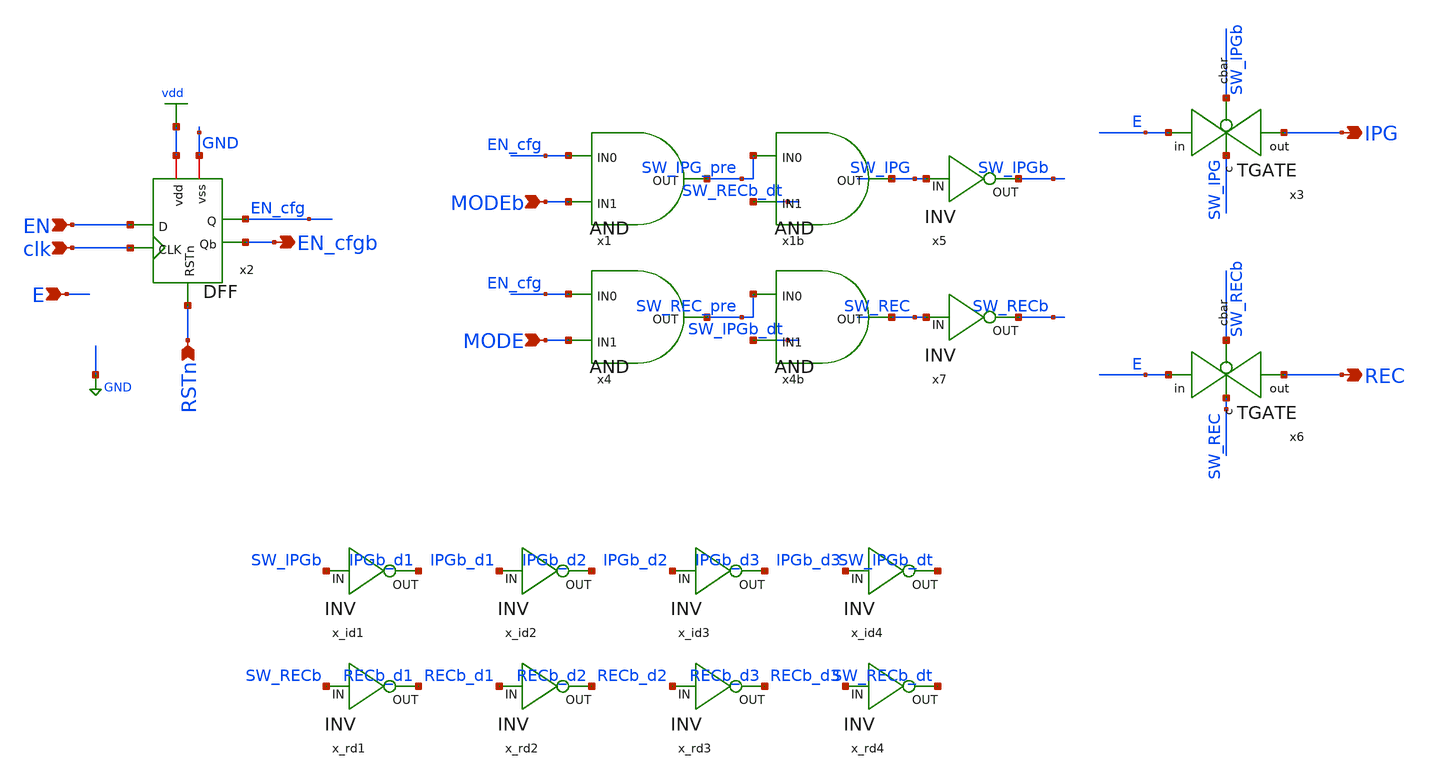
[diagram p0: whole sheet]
** sch_path: row_fixed_dt.sch
**.subckt row_fixed_dt EN clk MODEb MODE E IPG REC RSTn EN_cfgb
*.ipin EN
*.ipin clk
*.ipin MODEb
*.ipin MODE
*.ipin E
*.opin IPG
*.opin REC
*.ipin RSTn
*.opin EN_cfgb
x1 EN_cfg SW_IPG_pre MODEb AND
x2 vdd RSTn EN EN_cfg EN_cfgb clk GND DFF
x3 IPG SW_IPG SW_IPGb E TGATE
x4 EN_cfg SW_REC_pre MODE AND
x6 REC SW_REC SW_RECb E TGATE
x5 SW_IPGb SW_IPG INV
x7 SW_RECb SW_REC INV
x1b SW_IPG_pre SW_IPG SW_RECb_dt AND
x4b SW_REC_pre SW_REC SW_IPGb_dt AND
x_id1 IPGb_d1 SW_IPGb INV
x_id2 IPGb_d2 IPGb_d1 INV
x_id3 IPGb_d3 IPGb_d2 INV
x_id4 SW_IPGb_dt IPGb_d3 INV
x_rd1 RECb_d1 SW_RECb INV
x_rd2 RECb_d2 RECb_d1 INV
x_rd3 RECb_d3 RECb_d2 INV
x_rd4 SW_RECb_dt RECb_d3 INV
**.ends

* expanding   symbol:  AND/AND.sym # of pins=3
** sym_path: AND/AND.sym
** sch_path: AND/AND.sch
.subckt AND IN0 OUT IN1
*.opin OUT
*.ipin IN0
*.ipin IN1
XM1 net1 IN0 net2 GND nfet_03v3 L=0.28u W=1u nf=1 ad='int((nf+1)/2) * W/nf * 0.18u' as='int((nf+2)/2) * W/nf * 0.18u'
+ pd='2*int((nf+1)/2) * (W/nf + 0.18u)' ps='2*int((nf+2)/2) * (W/nf + 0.18u)' nrd='0.18u / W' nrs='0.18u / W'
+ sa=0 sb=0 sd=0 m=1
XM2 net2 IN1 GND GND nfet_03v3 L=0.28u W=1u nf=1 ad='int((nf+1)/2) * W/nf * 0.18u' as='int((nf+2)/2) * W/nf * 0.18u'
+ pd='2*int((nf+1)/2) * (W/nf + 0.18u)' ps='2*int((nf+2)/2) * (W/nf + 0.18u)' nrd='0.18u / W' nrs='0.18u / W'
+ sa=0 sb=0 sd=0 m=1
XM3 net1 IN0 vdd vdd pfet_03v3 L=0.28u W=1u nf=1 ad='int((nf+1)/2) * W/nf * 0.18u' as='int((nf+2)/2) * W/nf * 0.18u'
+ pd='2*int((nf+1)/2) * (W/nf + 0.18u)' ps='2*int((nf+2)/2) * (W/nf + 0.18u)' nrd='0.18u / W' nrs='0.18u / W'
+ sa=0 sb=0 sd=0 m=1
XM4 net1 IN1 vdd vdd pfet_03v3 L=0.28u W=1u nf=1 ad='int((nf+1)/2) * W/nf * 0.18u' as='int((nf+2)/2) * W/nf * 0.18u'
+ pd='2*int((nf+1)/2) * (W/nf + 0.18u)' ps='2*int((nf+2)/2) * (W/nf + 0.18u)' nrd='0.18u / W' nrs='0.18u / W'
+ sa=0 sb=0 sd=0 m=1
x1 OUT net1 INV
.ends


* expanding   symbol:  DFF/DFF.sym # of pins=7
** sym_path: DFF/DFF.sym
** sch_path: DFF/DFF.sch
.subckt DFF vdd RSTn D Q Qb CLK vss
*.ipin D
*.ipin CLK
*.ipin RSTn
*.opin Q
*.iopin vdd
*.iopin vss
*.opin Qb
XM1 net1 D net3 vss nfet_03v3 L=0.28u W=1u nf=1 ad='int((nf+1)/2) * W/nf * 0.18u' as='int((nf+2)/2) * W/nf * 0.18u'
+ pd='2*int((nf+1)/2) * (W/nf + 0.18u)' ps='2*int((nf+2)/2) * (W/nf + 0.18u)' nrd='0.18u / W' nrs='0.18u / W'
+ sa=0 sb=0 sd=0 m=1
XM2 net1 D net2 vdd pfet_03v3 L=0.28u W=1u nf=1 ad='int((nf+1)/2) * W/nf * 0.18u' as='int((nf+2)/2) * W/nf * 0.18u'
+ pd='2*int((nf+1)/2) * (W/nf + 0.18u)' ps='2*int((nf+2)/2) * (W/nf + 0.18u)' nrd='0.18u / W' nrs='0.18u / W'
+ sa=0 sb=0 sd=0 m=1
XM3 net2 c vdd vdd pfet_03v3 L=0.28u W=1u nf=1 ad='int((nf+1)/2) * W/nf * 0.18u' as='int((nf+2)/2) * W/nf * 0.18u'
+ pd='2*int((nf+1)/2) * (W/nf + 0.18u)' ps='2*int((nf+2)/2) * (W/nf + 0.18u)' nrd='0.18u / W' nrs='0.18u / W'
+ sa=0 sb=0 sd=0 m=1
XM4 net3 cbar vss vss nfet_03v3 L=0.28u W=1u nf=1 ad='int((nf+1)/2) * W/nf * 0.18u' as='int((nf+2)/2) * W/nf * 0.18u'
+ pd='2*int((nf+1)/2) * (W/nf + 0.18u)' ps='2*int((nf+2)/2) * (W/nf + 0.18u)' nrd='0.18u / W' nrs='0.18u / W'
+ sa=0 sb=0 sd=0 m=1
XM5 cbar CLK vss vss nfet_03v3 L=0.28u W=1u nf=1 ad='int((nf+1)/2) * W/nf * 0.18u' as='int((nf+2)/2) * W/nf * 0.18u'
+ pd='2*int((nf+1)/2) * (W/nf + 0.18u)' ps='2*int((nf+2)/2) * (W/nf + 0.18u)' nrd='0.18u / W' nrs='0.18u / W'
+ sa=0 sb=0 sd=0 m=1
XM6 cbar CLK vdd vdd pfet_03v3 L=0.28u W=1u nf=1 ad='int((nf+1)/2) * W/nf * 0.18u' as='int((nf+2)/2) * W/nf * 0.18u'
+ pd='2*int((nf+1)/2) * (W/nf + 0.18u)' ps='2*int((nf+2)/2) * (W/nf + 0.18u)' nrd='0.18u / W' nrs='0.18u / W'
+ sa=0 sb=0 sd=0 m=1
XM7 c cbar vss vss nfet_03v3 L=0.28u W=1u nf=1 ad='int((nf+1)/2) * W/nf * 0.18u' as='int((nf+2)/2) * W/nf * 0.18u'
+ pd='2*int((nf+1)/2) * (W/nf + 0.18u)' ps='2*int((nf+2)/2) * (W/nf + 0.18u)' nrd='0.18u / W' nrs='0.18u / W'
+ sa=0 sb=0 sd=0 m=1
XM8 c cbar vdd vdd pfet_03v3 L=0.28u W=1u nf=1 ad='int((nf+1)/2) * W/nf * 0.18u' as='int((nf+2)/2) * W/nf * 0.18u'
+ pd='2*int((nf+1)/2) * (W/nf + 0.18u)' ps='2*int((nf+2)/2) * (W/nf + 0.18u)' nrd='0.18u / W' nrs='0.18u / W'
+ sa=0 sb=0 sd=0 m=1
XM11 net5 RSTn net4 vss nfet_03v3 L=0.28u W=1u nf=1 ad='int((nf+1)/2) * W/nf * 0.18u' as='int((nf+2)/2) * W/nf * 0.18u'
+ pd='2*int((nf+1)/2) * (W/nf + 0.18u)' ps='2*int((nf+2)/2) * (W/nf + 0.18u)' nrd='0.18u / W' nrs='0.18u / W'
+ sa=0 sb=0 sd=0 m=1
XM12 net4 net6 vss vss nfet_03v3 L=0.28u W=1u nf=1 ad='int((nf+1)/2) * W/nf * 0.18u' as='int((nf+2)/2) * W/nf * 0.18u'
+ pd='2*int((nf+1)/2) * (W/nf + 0.18u)' ps='2*int((nf+2)/2) * (W/nf + 0.18u)' nrd='0.18u / W' nrs='0.18u / W'
+ sa=0 sb=0 sd=0 m=1
XM13 net5 RSTn vdd vdd pfet_03v3 L=0.28u W=1u nf=1 ad='int((nf+1)/2) * W/nf * 0.18u' as='int((nf+2)/2) * W/nf * 0.18u'
+ pd='2*int((nf+1)/2) * (W/nf + 0.18u)' ps='2*int((nf+2)/2) * (W/nf + 0.18u)' nrd='0.18u / W' nrs='0.18u / W'
+ sa=0 sb=0 sd=0 m=1
XM14 net5 net6 vdd vdd pfet_03v3 L=0.28u W=1u nf=1 ad='int((nf+1)/2) * W/nf * 0.18u' as='int((nf+2)/2) * W/nf * 0.18u'
+ pd='2*int((nf+1)/2) * (W/nf + 0.18u)' ps='2*int((nf+2)/2) * (W/nf + 0.18u)' nrd='0.18u / W' nrs='0.18u / W'
+ sa=0 sb=0 sd=0 m=1
XM15 net6 net1 vss vss nfet_03v3 L=0.28u W=1u nf=1 ad='int((nf+1)/2) * W/nf * 0.18u' as='int((nf+2)/2) * W/nf * 0.18u'
+ pd='2*int((nf+1)/2) * (W/nf + 0.18u)' ps='2*int((nf+2)/2) * (W/nf + 0.18u)' nrd='0.18u / W' nrs='0.18u / W'
+ sa=0 sb=0 sd=0 m=1
XM16 net6 net1 vdd vdd pfet_03v3 L=0.28u W=1u nf=1 ad='int((nf+1)/2) * W/nf * 0.18u' as='int((nf+2)/2) * W/nf * 0.18u'
+ pd='2*int((nf+1)/2) * (W/nf + 0.18u)' ps='2*int((nf+2)/2) * (W/nf + 0.18u)' nrd='0.18u / W' nrs='0.18u / W'
+ sa=0 sb=0 sd=0 m=1
XM21 net9 net7 net8 vss nfet_03v3 L=0.28u W=1u nf=1 ad='int((nf+1)/2) * W/nf * 0.18u' as='int((nf+2)/2) * W/nf * 0.18u'
+ pd='2*int((nf+1)/2) * (W/nf + 0.18u)' ps='2*int((nf+2)/2) * (W/nf + 0.18u)' nrd='0.18u / W' nrs='0.18u / W'
+ sa=0 sb=0 sd=0 m=1
XM22 net8 RSTn vss vss nfet_03v3 L=0.28u W=1u nf=1 ad='int((nf+1)/2) * W/nf * 0.18u' as='int((nf+2)/2) * W/nf * 0.18u'
+ pd='2*int((nf+1)/2) * (W/nf + 0.18u)' ps='2*int((nf+2)/2) * (W/nf + 0.18u)' nrd='0.18u / W' nrs='0.18u / W'
+ sa=0 sb=0 sd=0 m=1
XM23 net9 net7 vdd vdd pfet_03v3 L=0.28u W=1u nf=1 ad='int((nf+1)/2) * W/nf * 0.18u' as='int((nf+2)/2) * W/nf * 0.18u'
+ pd='2*int((nf+1)/2) * (W/nf + 0.18u)' ps='2*int((nf+2)/2) * (W/nf + 0.18u)' nrd='0.18u / W' nrs='0.18u / W'
+ sa=0 sb=0 sd=0 m=1
XM24 net9 RSTn vdd vdd pfet_03v3 L=0.28u W=1u nf=1 ad='int((nf+1)/2) * W/nf * 0.18u' as='int((nf+2)/2) * W/nf * 0.18u'
+ pd='2*int((nf+1)/2) * (W/nf + 0.18u)' ps='2*int((nf+2)/2) * (W/nf + 0.18u)' nrd='0.18u / W' nrs='0.18u / W'
+ sa=0 sb=0 sd=0 m=1
XM25 Q net9 vss vss nfet_03v3 L=0.28u W=1u nf=1 ad='int((nf+1)/2) * W/nf * 0.18u' as='int((nf+2)/2) * W/nf * 0.18u'
+ pd='2*int((nf+1)/2) * (W/nf + 0.18u)' ps='2*int((nf+2)/2) * (W/nf + 0.18u)' nrd='0.18u / W' nrs='0.18u / W'
+ sa=0 sb=0 sd=0 m=1
XM26 Q net9 vdd vdd pfet_03v3 L=0.28u W=1u nf=1 ad='int((nf+1)/2) * W/nf * 0.18u' as='int((nf+2)/2) * W/nf * 0.18u'
+ pd='2*int((nf+1)/2) * (W/nf + 0.18u)' ps='2*int((nf+2)/2) * (W/nf + 0.18u)' nrd='0.18u / W' nrs='0.18u / W'
+ sa=0 sb=0 sd=0 m=1
XM19 net7 net9 net11 vss nfet_03v3 L=0.28u W=1u nf=1 ad='int((nf+1)/2) * W/nf * 0.18u' as='int((nf+2)/2) * W/nf * 0.18u'
+ pd='2*int((nf+1)/2) * (W/nf + 0.18u)' ps='2*int((nf+2)/2) * (W/nf + 0.18u)' nrd='0.18u / W' nrs='0.18u / W'
+ sa=0 sb=0 sd=0 m=1
XM20 net7 net9 net10 vdd pfet_03v3 L=0.28u W=1u nf=1 ad='int((nf+1)/2) * W/nf * 0.18u' as='int((nf+2)/2) * W/nf * 0.18u'
+ pd='2*int((nf+1)/2) * (W/nf + 0.18u)' ps='2*int((nf+2)/2) * (W/nf + 0.18u)' nrd='0.18u / W' nrs='0.18u / W'
+ sa=0 sb=0 sd=0 m=1
XM31 net10 c vdd vdd pfet_03v3 L=0.28u W=1u nf=1 ad='int((nf+1)/2) * W/nf * 0.18u' as='int((nf+2)/2) * W/nf * 0.18u'
+ pd='2*int((nf+1)/2) * (W/nf + 0.18u)' ps='2*int((nf+2)/2) * (W/nf + 0.18u)' nrd='0.18u / W' nrs='0.18u / W'
+ sa=0 sb=0 sd=0 m=1
XM32 net11 cbar vss vss nfet_03v3 L=0.28u W=1u nf=1 ad='int((nf+1)/2) * W/nf * 0.18u' as='int((nf+2)/2) * W/nf * 0.18u'
+ pd='2*int((nf+1)/2) * (W/nf + 0.18u)' ps='2*int((nf+2)/2) * (W/nf + 0.18u)' nrd='0.18u / W' nrs='0.18u / W'
+ sa=0 sb=0 sd=0 m=1
XM35 net12 net9 vss vss nfet_03v3 L=0.28u W=1u nf=1 ad='int((nf+1)/2) * W/nf * 0.18u' as='int((nf+2)/2) * W/nf * 0.18u'
+ pd='2*int((nf+1)/2) * (W/nf + 0.18u)' ps='2*int((nf+2)/2) * (W/nf + 0.18u)' nrd='0.18u / W' nrs='0.18u / W'
+ sa=0 sb=0 sd=0 m=1
XM36 net12 net9 vdd vdd pfet_03v3 L=0.28u W=1u nf=1 ad='int((nf+1)/2) * W/nf * 0.18u' as='int((nf+2)/2) * W/nf * 0.18u'
+ pd='2*int((nf+1)/2) * (W/nf + 0.18u)' ps='2*int((nf+2)/2) * (W/nf + 0.18u)' nrd='0.18u / W' nrs='0.18u / W'
+ sa=0 sb=0 sd=0 m=1
XM37 Qb net12 vss vss nfet_03v3 L=0.28u W=1u nf=1 ad='int((nf+1)/2) * W/nf * 0.18u' as='int((nf+2)/2) * W/nf * 0.18u'
+ pd='2*int((nf+1)/2) * (W/nf + 0.18u)' ps='2*int((nf+2)/2) * (W/nf + 0.18u)' nrd='0.18u / W' nrs='0.18u / W'
+ sa=0 sb=0 sd=0 m=1
XM38 Qb net12 vdd vdd pfet_03v3 L=0.28u W=1u nf=1 ad='int((nf+1)/2) * W/nf * 0.18u' as='int((nf+2)/2) * W/nf * 0.18u'
+ pd='2*int((nf+1)/2) * (W/nf + 0.18u)' ps='2*int((nf+2)/2) * (W/nf + 0.18u)' nrd='0.18u / W' nrs='0.18u / W'
+ sa=0 sb=0 sd=0 m=1
XM9 net1 c net5 vss nfet_03v3 L=0.28u W=1u nf=1 ad='int((nf+1)/2) * W/nf * 0.18u' as='int((nf+2)/2) * W/nf * 0.18u'
+ pd='2*int((nf+1)/2) * (W/nf + 0.18u)' ps='2*int((nf+2)/2) * (W/nf + 0.18u)' nrd='0.18u / W' nrs='0.18u / W'
+ sa=0 sb=0 sd=0 m=1
XM10 net1 cbar net5 vdd pfet_03v3 L=0.28u W=1u nf=1 ad='int((nf+1)/2) * W/nf * 0.18u' as='int((nf+2)/2) * W/nf * 0.18u'
+ pd='2*int((nf+1)/2) * (W/nf + 0.18u)' ps='2*int((nf+2)/2) * (W/nf + 0.18u)' nrd='0.18u / W' nrs='0.18u / W'
+ sa=0 sb=0 sd=0 m=1
XM17 net6 c net7 vss nfet_03v3 L=0.28u W=1u nf=1 ad='int((nf+1)/2) * W/nf * 0.18u' as='int((nf+2)/2) * W/nf * 0.18u'
+ pd='2*int((nf+1)/2) * (W/nf + 0.18u)' ps='2*int((nf+2)/2) * (W/nf + 0.18u)' nrd='0.18u / W' nrs='0.18u / W'
+ sa=0 sb=0 sd=0 m=1
XM18 net6 cbar net7 vdd pfet_03v3 L=0.28u W=1u nf=1 ad='int((nf+1)/2) * W/nf * 0.18u' as='int((nf+2)/2) * W/nf * 0.18u'
+ pd='2*int((nf+1)/2) * (W/nf + 0.18u)' ps='2*int((nf+2)/2) * (W/nf + 0.18u)' nrd='0.18u / W' nrs='0.18u / W'
+ sa=0 sb=0 sd=0 m=1
.ends


* expanding   symbol:  TGATE/TGATE.sym # of pins=4
** sym_path: TGATE/TGATE.sym
** sch_path: TGATE/TGATE.sch
.subckt TGATE out c cbar in
*.ipin in
*.opin out
*.ipin cbar
*.ipin c
XM1 out cbar in VDD pfet_03v3 L=0.28u W=1u nf=1 ad='int((nf+1)/2) * W/nf * 0.18u' as='int((nf+2)/2) * W/nf * 0.18u'
+ pd='2*int((nf+1)/2) * (W/nf + 0.18u)' ps='2*int((nf+2)/2) * (W/nf + 0.18u)' nrd='0.18u / W' nrs='0.18u / W'
+ sa=0 sb=0 sd=0 m=1
XM2 out c in GND nfet_03v3 L=0.28u W=1u nf=1 ad='int((nf+1)/2) * W/nf * 0.18u' as='int((nf+2)/2) * W/nf * 0.18u'
+ pd='2*int((nf+1)/2) * (W/nf + 0.18u)' ps='2*int((nf+2)/2) * (W/nf + 0.18u)' nrd='0.18u / W' nrs='0.18u / W'
+ sa=0 sb=0 sd=0 m=1
.ends


* expanding   symbol:  AND/INV.sym # of pins=2
** sym_path: AND/INV.sym
** sch_path: AND/INV.sch
.subckt INV OUT IN
*.ipin IN
*.opin OUT
XM1 OUT IN VDD VDD pfet_03v3 L=0.28u W=1u nf=1 ad='int((nf+1)/2) * W/nf * 0.18u' as='int((nf+2)/2) * W/nf * 0.18u'
+ pd='2*int((nf+1)/2) * (W/nf + 0.18u)' ps='2*int((nf+2)/2) * (W/nf + 0.18u)' nrd='0.18u / W' nrs='0.18u / W'
+ sa=0 sb=0 sd=0 m=1
XM2 OUT IN GND GND nfet_03v3 L=0.28u W=0.5u nf=1 ad='int((nf+1)/2) * W/nf * 0.18u' as='int((nf+2)/2) * W/nf * 0.18u'
+ pd='2*int((nf+1)/2) * (W/nf + 0.18u)' ps='2*int((nf+2)/2) * (W/nf + 0.18u)' nrd='0.18u / W' nrs='0.18u / W'
+ sa=0 sb=0 sd=0 m=1
.ends

.GLOBAL GND
.GLOBAL vdd
.GLOBAL VDD
.end
